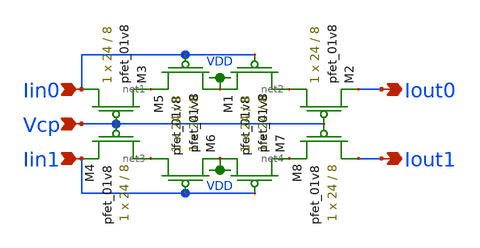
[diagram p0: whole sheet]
** sch_path: modules/cascode_mirror_lds.sch
**.subckt cascode_mirror_lds Vcp Iin0 Iout0 Iin1 Iout1
*.ipin Vcp
*.ipin Iin0
*.opin Iout0
*.ipin Iin1
*.opin Iout1
XM5 VDD Iin0 net1 VDD sky130_fd_pr__pfet_01v8 L=8 W=24 nf=1 ad='int((nf+1)/2) * W/nf * 0.29' as='int((nf+2)/2) * W/nf * 0.29'
+ pd='2*int((nf+1)/2) * (W/nf + 0.29)' ps='2*int((nf+2)/2) * (W/nf + 0.29)' nrd='0.29 / W' nrs='0.29 / W'
+ sa=0 sb=0 sd=0 mult=1 m=1
XM1 net2 Iin0 VDD VDD sky130_fd_pr__pfet_01v8 L=8 W=24 nf=1 ad='int((nf+1)/2) * W/nf * 0.29' as='int((nf+2)/2) * W/nf * 0.29'
+ pd='2*int((nf+1)/2) * (W/nf + 0.29)' ps='2*int((nf+2)/2) * (W/nf + 0.29)' nrd='0.29 / W' nrs='0.29 / W'
+ sa=0 sb=0 sd=0 mult=1 m=1
XM2 net2 Vcp Iout0 VDD sky130_fd_pr__pfet_01v8 L=8 W=24 nf=1 ad='int((nf+1)/2) * W/nf * 0.29' as='int((nf+2)/2) * W/nf * 0.29'
+ pd='2*int((nf+1)/2) * (W/nf + 0.29)' ps='2*int((nf+2)/2) * (W/nf + 0.29)' nrd='0.29 / W' nrs='0.29 / W'
+ sa=0 sb=0 sd=0 mult=1 m=1
XM3 Iin0 Vcp net1 VDD sky130_fd_pr__pfet_01v8 L=8 W=24 nf=1 ad='int((nf+1)/2) * W/nf * 0.29' as='int((nf+2)/2) * W/nf * 0.29'
+ pd='2*int((nf+1)/2) * (W/nf + 0.29)' ps='2*int((nf+2)/2) * (W/nf + 0.29)' nrd='0.29 / W' nrs='0.29 / W'
+ sa=0 sb=0 sd=0 mult=1 m=1
XM4 net3 Vcp Iin1 VDD sky130_fd_pr__pfet_01v8 L=8 W=24 nf=1 ad='int((nf+1)/2) * W/nf * 0.29' as='int((nf+2)/2) * W/nf * 0.29'
+ pd='2*int((nf+1)/2) * (W/nf + 0.29)' ps='2*int((nf+2)/2) * (W/nf + 0.29)' nrd='0.29 / W' nrs='0.29 / W'
+ sa=0 sb=0 sd=0 mult=1 m=1
XM6 net3 Iin1 VDD VDD sky130_fd_pr__pfet_01v8 L=8 W=24 nf=1 ad='int((nf+1)/2) * W/nf * 0.29' as='int((nf+2)/2) * W/nf * 0.29'
+ pd='2*int((nf+1)/2) * (W/nf + 0.29)' ps='2*int((nf+2)/2) * (W/nf + 0.29)' nrd='0.29 / W' nrs='0.29 / W'
+ sa=0 sb=0 sd=0 mult=1 m=1
XM7 VDD Iin1 net4 VDD sky130_fd_pr__pfet_01v8 L=8 W=24 nf=1 ad='int((nf+1)/2) * W/nf * 0.29' as='int((nf+2)/2) * W/nf * 0.29'
+ pd='2*int((nf+1)/2) * (W/nf + 0.29)' ps='2*int((nf+2)/2) * (W/nf + 0.29)' nrd='0.29 / W' nrs='0.29 / W'
+ sa=0 sb=0 sd=0 mult=1 m=1
XM8 Iout1 Vcp net4 VDD sky130_fd_pr__pfet_01v8 L=8 W=24 nf=1 ad='int((nf+1)/2) * W/nf * 0.29' as='int((nf+2)/2) * W/nf * 0.29'
+ pd='2*int((nf+1)/2) * (W/nf + 0.29)' ps='2*int((nf+2)/2) * (W/nf + 0.29)' nrd='0.29 / W' nrs='0.29 / W'
+ sa=0 sb=0 sd=0 mult=1 m=1
**.ends
.GLOBAL VDD
.end
